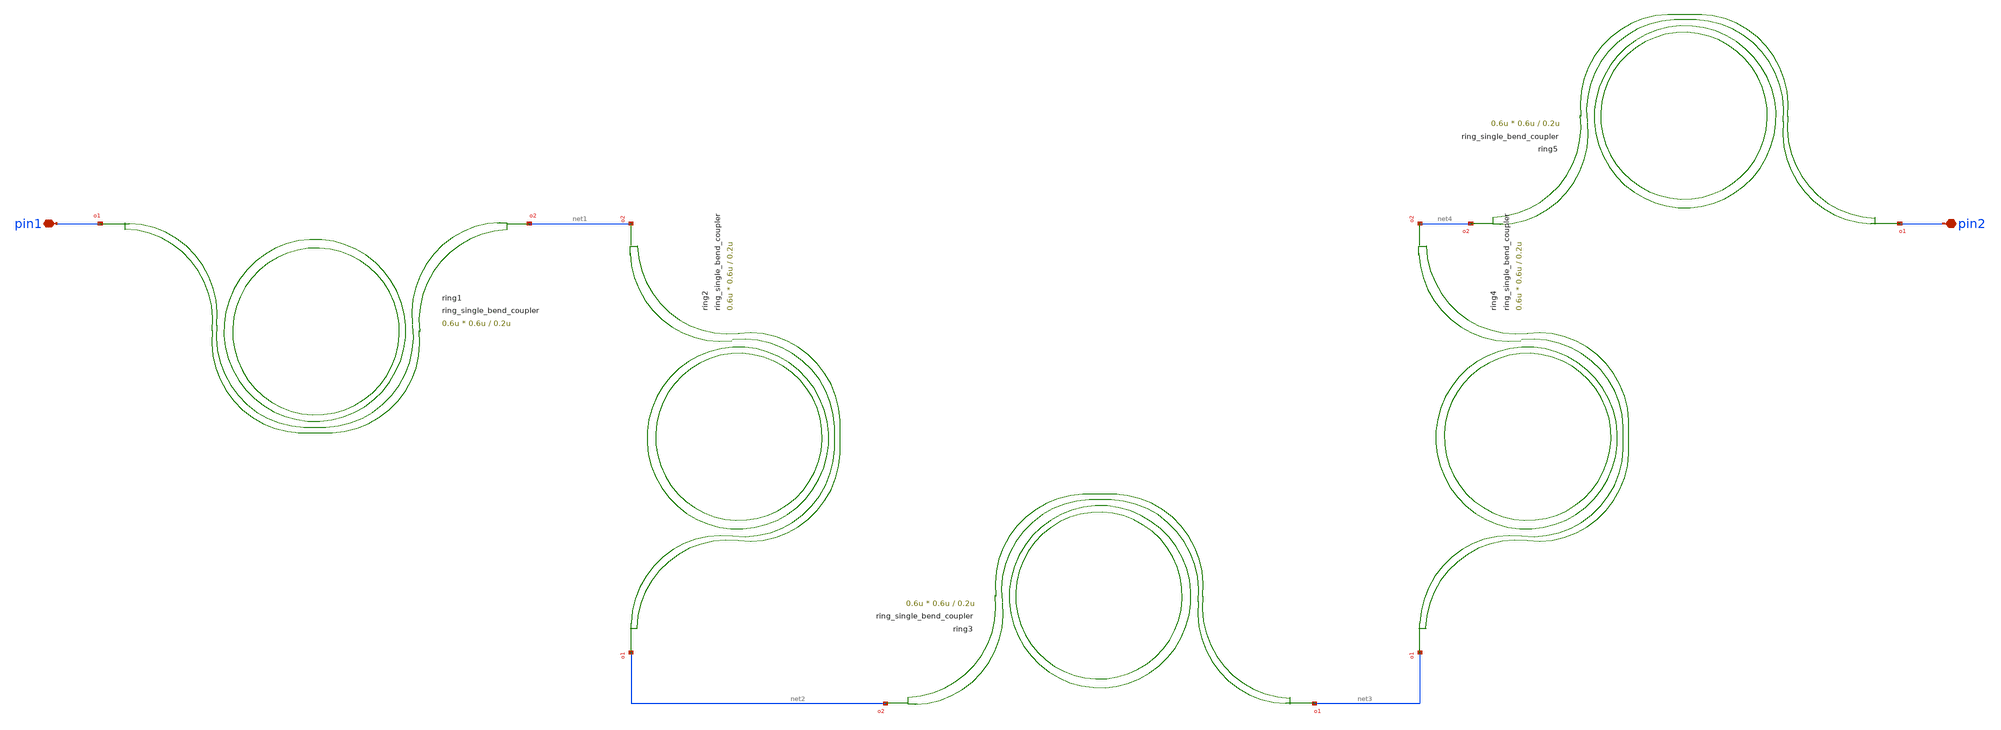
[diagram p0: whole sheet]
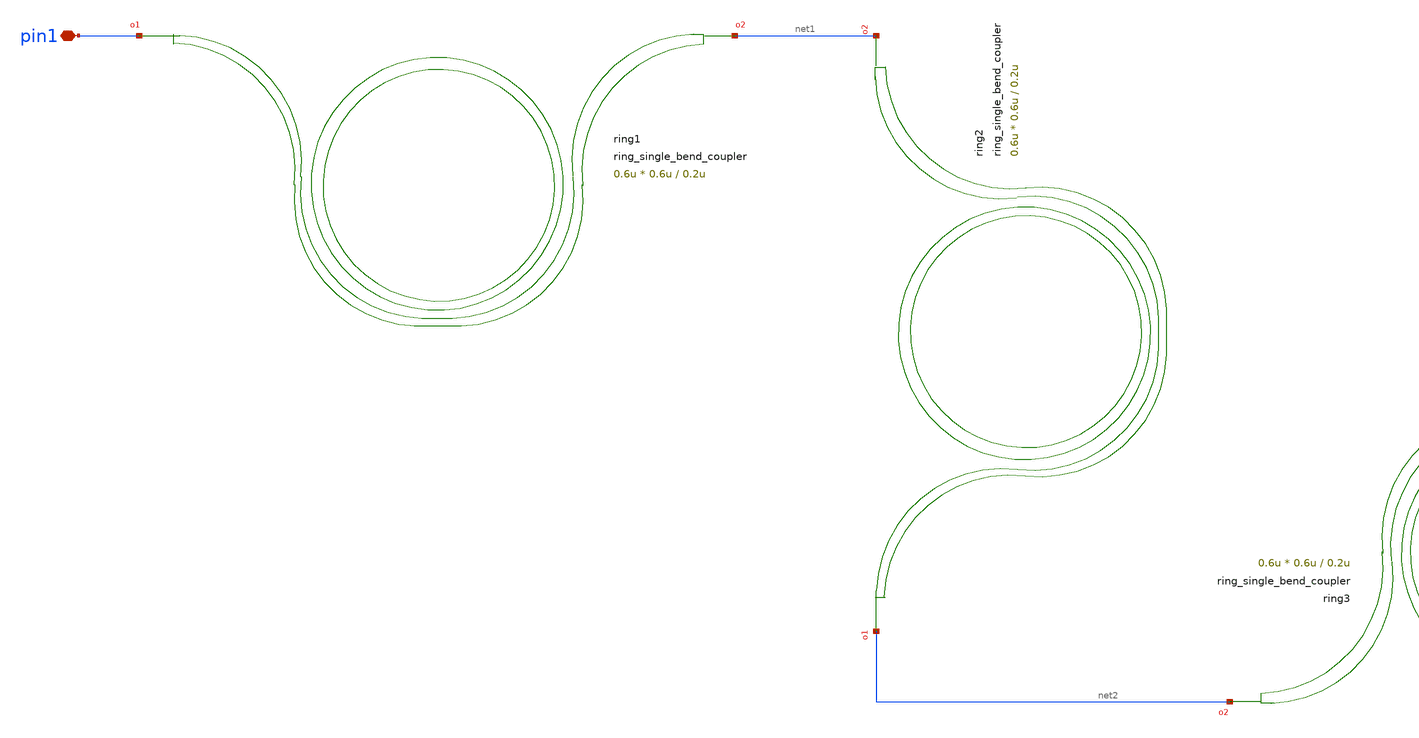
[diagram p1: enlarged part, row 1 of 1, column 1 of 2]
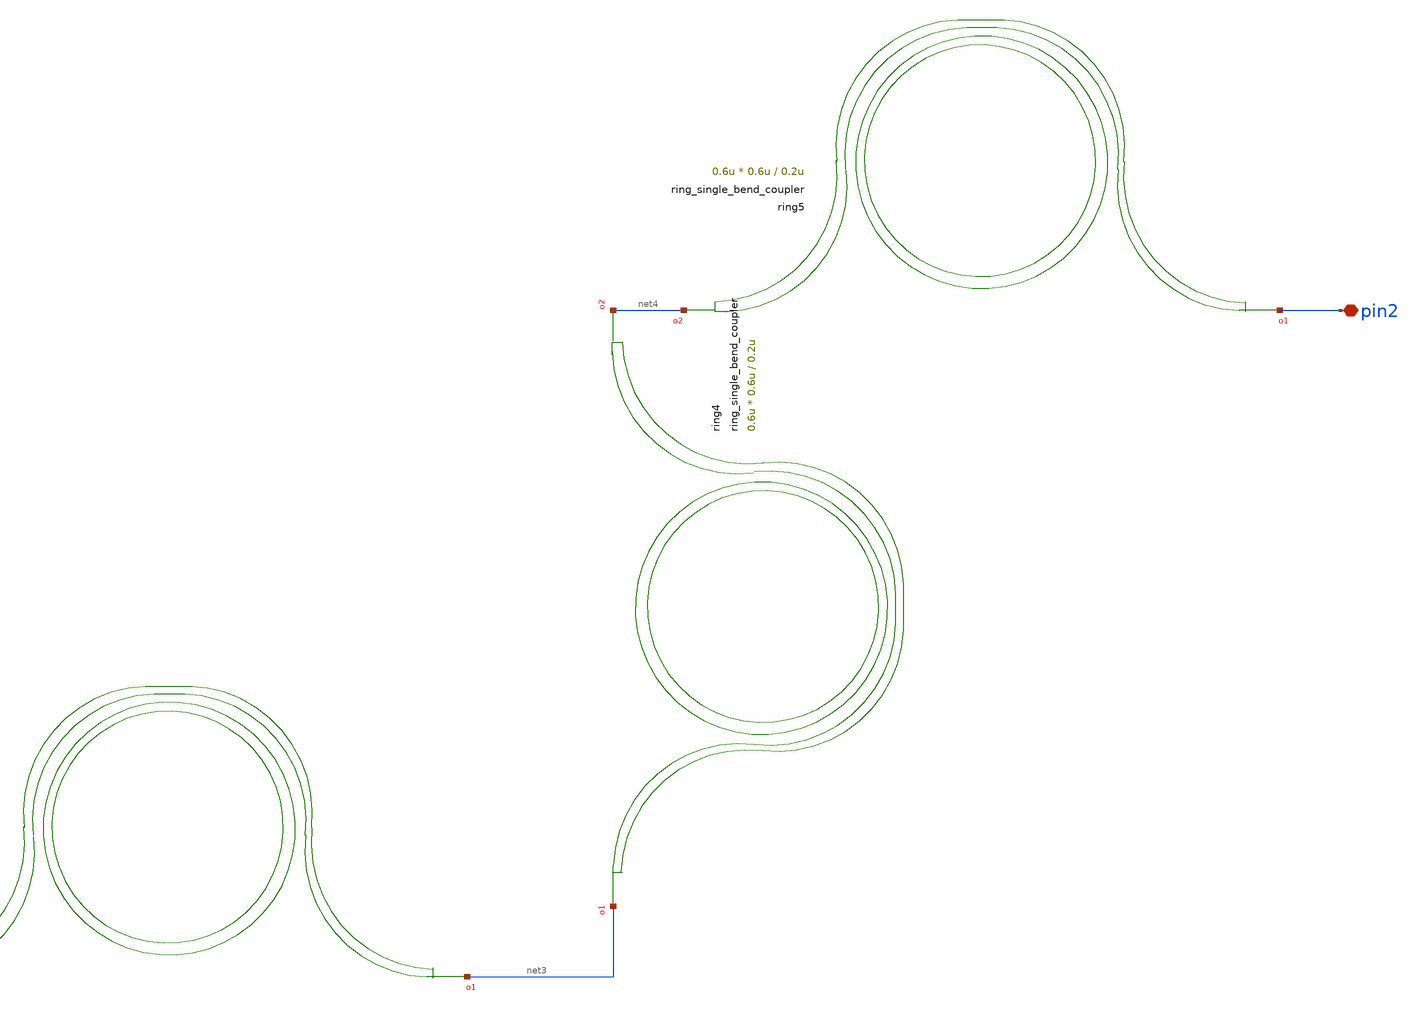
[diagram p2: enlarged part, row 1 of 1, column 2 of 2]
** sch_path: xschem/tests/test_sch/test_ring_single_bend_coupler.sch
* Copyright (c) 2024, Mabrains LLC
* Licensed under the GNU Lesser General Public License, Version 3.0 (the "License");
* you may not use this file except in compliance with the License.
* GNU Lesser General Public License
* Version 3, 29 June 2007
* This program is free software: you can redistribute it and/or modify
* it under the terms of the GNU Lesser General Public License as published
* by the Free Software Foundation, either version 3 of the License, or
* (at your option) any later version.
* This program is distributed in the hope that it will be useful,
* but WITHOUT ANY WARRANTY; without even the implied warranty of
* MERCHANTABILITY or FITNESS FOR A PARTICULAR PURPOSE.  See the
* GNU Lesser General Public License for more details.
* You should have received a copy of the GNU Lesser General Public License
* along with this program.  If not, see <https://www.gnu.org/licenses/>.
* SPDX-License-Identifier: LGPL-3.0
**.subckt test_ring_single_bend_coupler pin1 pin2
*.iopin pin1
*.iopin pin2
Pring1 pin1 net1 ring_single_bend_coupler gap=0.2u radius=5.0u angle_inner=90 angle_outer=90
+ length_x=0.6u length_y=0.6u
Pring2 net2 net1 ring_single_bend_coupler gap=0.2u radius=5.0u angle_inner=90 angle_outer=90
+ length_x=0.6u length_y=0.6u
Pring3 net3 net2 ring_single_bend_coupler gap=0.2u radius=5.0u angle_inner=90 angle_outer=90
+ length_x=0.6u length_y=0.6u
Pring4 net3 net4 ring_single_bend_coupler gap=0.2u radius=5.0u angle_inner=90 angle_outer=90
+ length_x=0.6u length_y=0.6u
Pring5 pin2 net4 ring_single_bend_coupler gap=0.2u radius=5.0u angle_inner=90 angle_outer=90
+ length_x=0.6u length_y=0.6u
**.ends
.end
